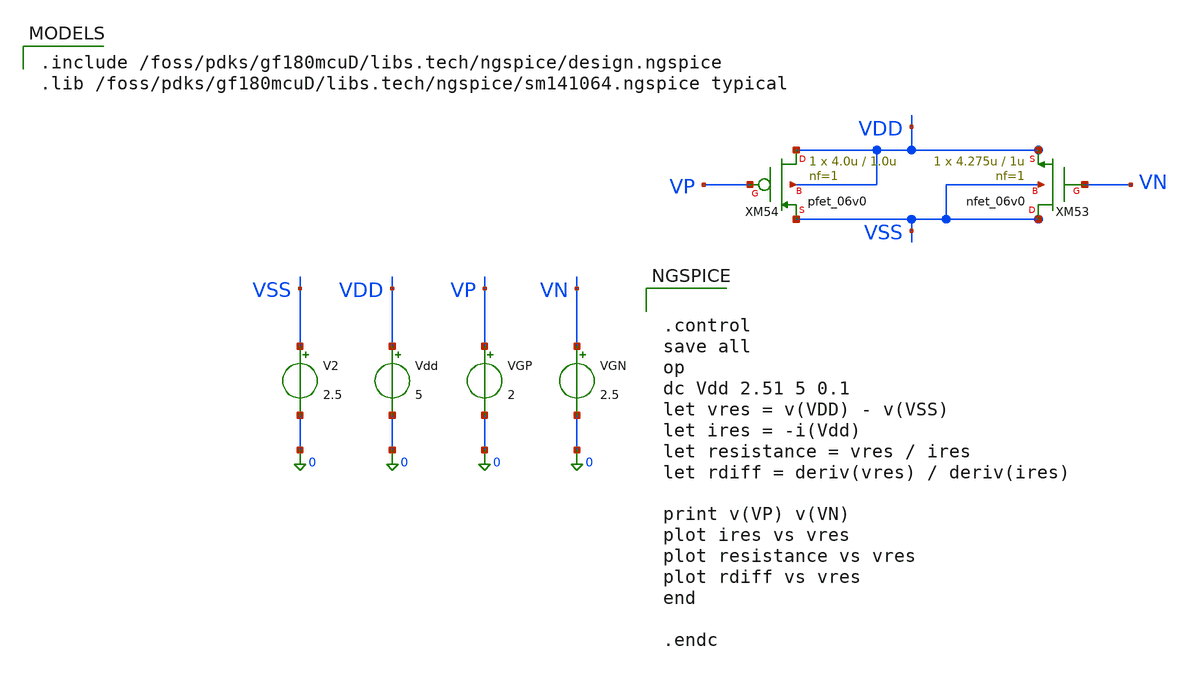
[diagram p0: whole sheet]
** sch_path: activities/opamp3An/RfLinearityCheck.sch
**.subckt RfLinearityCheck
XM53 VSS VN VDD VSS nfet_06v0 L=1u W=4.275u nf=1 ad='int((nf+1)/2) * W/nf * 0.18u' as='int((nf+2)/2) * W/nf * 0.18u'
+ pd='2*int((nf+1)/2) * (W/nf + 0.18u)' ps='2*int((nf+2)/2) * (W/nf + 0.18u)' nrd='0.18u / W' nrs='0.18u / W'
+ sa=0 sb=0 sd=0 m=1
XM54 VDD VP VSS VDD pfet_06v0 L=1.0u W=4.0u nf=1 ad='int((nf+1)/2) * W/nf * 0.18u' as='int((nf+2)/2) * W/nf * 0.18u'
+ pd='2*int((nf+1)/2) * (W/nf + 0.18u)' ps='2*int((nf+2)/2) * (W/nf + 0.18u)' nrd='0.18u / W' nrs='0.18u / W'
+ sa=0 sb=0 sd=0 m=1
V2 VSS 0 2.5
Vdd VDD 0 5
VGP VP 0 2
VGN VN 0 2.5
**** begin user architecture code

.include /foss/pdks/gf180mcuD/libs.tech/ngspice/design.ngspice
.lib /foss/pdks/gf180mcuD/libs.tech/ngspice/sm141064.ngspice typical



.control
save all
op
dc Vdd 2.51 5 0.1
let vres = v(VDD) - v(VSS)
let ires = -i(Vdd)
let resistance = vres / ires
let rdiff = deriv(vres) / deriv(ires)

print v(VP) v(VN)
plot ires vs vres
plot resistance vs vres
plot rdiff vs vres
end

.endc

**** end user architecture code
**.ends
.end
